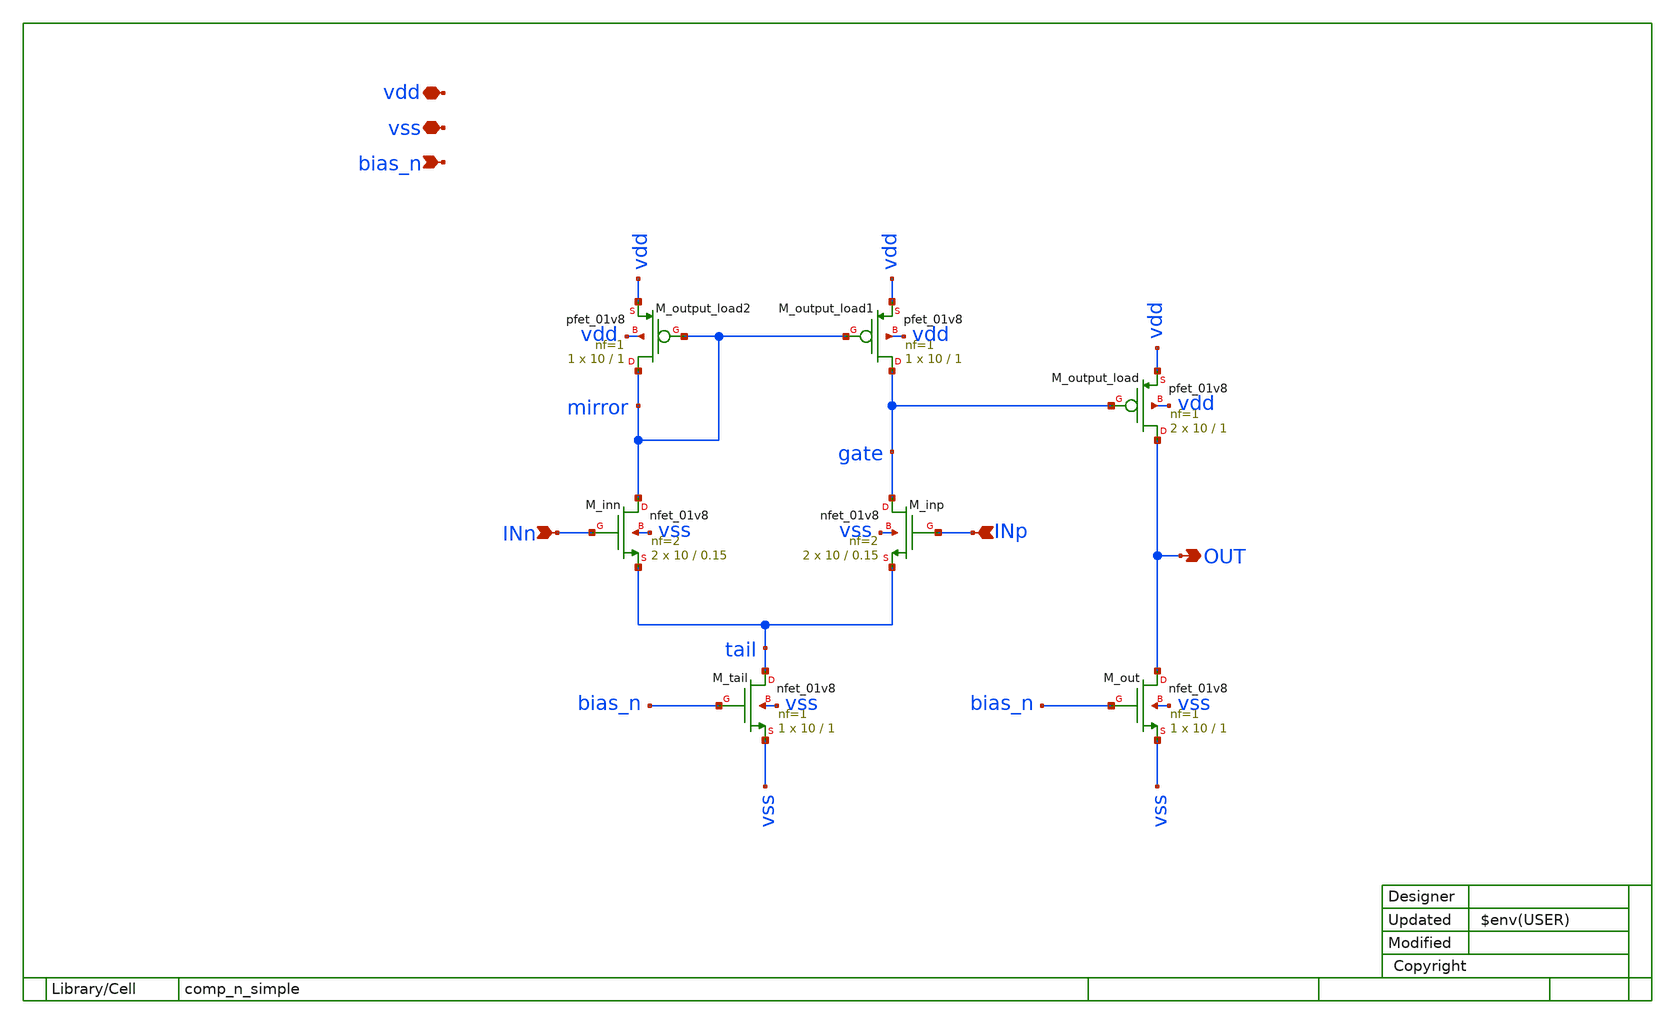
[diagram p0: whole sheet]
** sch_path: xsch/ip/zzOLD/comp_n_simple.sch
**.subckt comp_n_simple vdd OUT vss bias_n INn INp
*.iopin vdd
*.opin OUT
*.iopin vss
*.ipin bias_n
*.ipin INn
*.ipin INp
XM_tail tail bias_n vss vss sky130_fd_pr__nfet_01v8 L=1 W=10 nf=1 ad='int((1 + 1)/2) * 10 / 1 * 0.29'
+ as='int((1 + 2)/2) * 10 / 1 * 0.29' pd='2*int((1 + 1)/2) * (10 / 1 + 0.29)' ps='2*int((1 + 2)/2) * (10 / 1 + 0.29)'
+ nrd='0.29 / 10 ' nrs='0.29 / 10 ' sa=0 sb=0 sd=0 mult=1 m=1
XM_out OUT bias_n vss vss sky130_fd_pr__nfet_01v8 L=1 W=10 nf=1 ad='int((1 + 1)/2) * 10 / 1 * 0.29' as='int((1 + 2)/2) * 10 / 1 * 0.29'
+ pd='2*int((1 + 1)/2) * (10 / 1 + 0.29)' ps='2*int((1 + 2)/2) * (10 / 1 + 0.29)' nrd='0.29 / 10 ' nrs='0.29 / 10 '
+ sa=0 sb=0 sd=0 mult=1 m=1
XM_output_load OUT gate vdd vdd sky130_fd_pr__pfet_01v8 L=1 W=10 nf=1 ad='int((nf+1)/2) * W/nf * 0.29'
+ as='int((nf+2)/2) * W/nf * 0.29' pd='2*int((nf+1)/2) * (W/nf + 0.29)' ps='2*int((nf+2)/2) * (W/nf + 0.29)'
+ nrd='0.29 / W' nrs='0.29 / W' sa=0 sb=0 sd=0 mult=2 m=2
XM_inn mirror INn tail vss sky130_fd_pr__nfet_01v8 L=0.15 W=10 nf=2 ad='int((2 + 1)/2) * 10 / 2 * 0.29'
+ as='int((2 + 2)/2) * 10 / 2 * 0.29' pd='2*int((2 + 1)/2) * (10 / 2 + 0.29)' ps='2*int((2 + 2)/2) * (10 / 2 + 0.29)'
+ nrd='0.29 / 10 ' nrs='0.29 / 10 ' sa=0 sb=0 sd=0 mult=2 m=2
XM_inp gate INp tail vss sky130_fd_pr__nfet_01v8 L=0.15 W=10 nf=2 ad='int((2 + 1)/2) * 10 / 2 * 0.29'
+ as='int((2 + 2)/2) * 10 / 2 * 0.29' pd='2*int((2 + 1)/2) * (10 / 2 + 0.29)' ps='2*int((2 + 2)/2) * (10 / 2 + 0.29)'
+ nrd='0.29 / 10 ' nrs='0.29 / 10 ' sa=0 sb=0 sd=0 mult=2 m=2
XM_output_load1 gate mirror vdd vdd sky130_fd_pr__pfet_01v8 L=1 W=10 nf=1 ad='int((nf+1)/2) * W/nf * 0.29'
+ as='int((nf+2)/2) * W/nf * 0.29' pd='2*int((nf+1)/2) * (W/nf + 0.29)' ps='2*int((nf+2)/2) * (W/nf + 0.29)'
+ nrd='0.29 / W' nrs='0.29 / W' sa=0 sb=0 sd=0 mult=1 m=1
XM_output_load2 mirror mirror vdd vdd sky130_fd_pr__pfet_01v8 L=1 W=10 nf=1 ad='int((nf+1)/2) * W/nf * 0.29'
+ as='int((nf+2)/2) * W/nf * 0.29' pd='2*int((nf+1)/2) * (W/nf + 0.29)' ps='2*int((nf+2)/2) * (W/nf + 0.29)'
+ nrd='0.29 / W' nrs='0.29 / W' sa=0 sb=0 sd=0 mult=1 m=1
**.ends
.end
